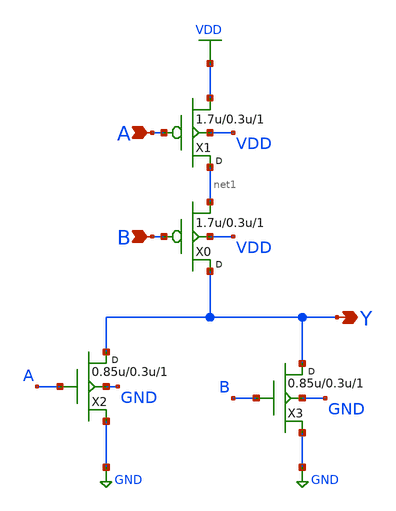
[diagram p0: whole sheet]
** sch_path: openfasoc/common/platforms/gf180mcuosu9Tnor21/gf180mcu_osu_sc_nor2_1.sch
**.subckt gf180mcu_osu_sc_nor2_1 A B Y
*.ipin A
*.ipin B
*.opin Y
X1 net1 A VDD VDD pmos_3p3 w=1.7u l=0.3u m=1
X0 Y B net1 VDD pmos_3p3 w=1.7u l=0.3u m=1
X2 Y A GND GND nmos_3p3 w=0.85u l=0.3u m=1
X3 Y B GND GND nmos_3p3 w=0.85u l=0.3u m=1
**.ends
.GLOBAL VDD
.GLOBAL GND
.end
